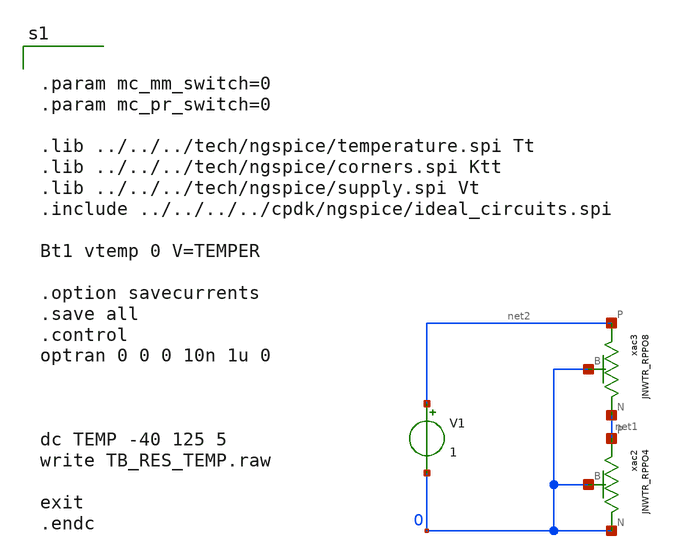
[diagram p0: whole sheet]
** sch_path: design/LELO_TEMP_SKY130A/TB_RES_TEMP.sch
**.subckt TB_RES_TEMP
xac2 0 net1 0 JNWTR_RPPO4 xoffset=0 yoffset=0 angle=0
xac3 net1 net2 0 JNWTR_RPPO8 xoffset=0 yoffset=0 angle=0 M=1
V1 net2 0 1
**** begin user architecture code


.param mc_mm_switch=0
.param mc_pr_switch=0

.lib ../../../tech/ngspice/temperature.spi Tt
.lib ../../../tech/ngspice/corners.spi Ktt
.lib ../../../tech/ngspice/supply.spi Vt
.include ../../../../cpdk/ngspice/ideal_circuits.spi

Bt1 vtemp 0 V=TEMPER

.option savecurrents
.save all
.control
optran 0 0 0 10n 1u 0



dc TEMP -40 125 5
write TB_RES_TEMP.raw

exit
.endc



**** end user architecture code
**.ends

* expanding   symbol:  JNW_TR_SKY130A/JNWTR_RPPO4.sym # of pins=3
** sym_path: JNW_TR_SKY130A/JNWTR_RPPO4.sym
** sch_path: JNW_TR_SKY130A/JNWTR_RPPO4.sch
.subckt JNWTR_RPPO4 N P B  xoffset=0 yoffset=0 angle=0
*.iopin P
*.iopin N
*.iopin B
XXA1 N P B JNWTR_RES4
.ends


* expanding   symbol:  JNW_TR_SKY130A/JNWTR_RPPO8.sym # of pins=3
** sym_path: JNW_TR_SKY130A/JNWTR_RPPO8.sym
** sch_path: JNW_TR_SKY130A/JNWTR_RPPO8.sch
.subckt JNWTR_RPPO8 N P B  xoffset=0 yoffset=0 angle=0 M=1
*.iopin P
*.iopin N
*.iopin B
XXA1 N P B JNWTR_RES8 xoffset=0 yoffset=0 angle=0
.ends


* expanding   symbol:  JNW_TR_SKY130A/JNWTR_RES4.sym # of pins=3
** sym_path: JNW_TR_SKY130A/JNWTR_RES4.sym
** sch_path: JNW_TR_SKY130A/JNWTR_RES4.sch
.subckt JNWTR_RES4 N P B
*.iopin N
*.iopin P
*.iopin B
XR1_0 INT_0 N B sky130_fd_pr__res_high_po W=0.36 L=7.2 mult=1 m=1
XR1_1 INT_1 INT_0 B sky130_fd_pr__res_high_po W=0.36 L=7.2 mult=1 m=1
XR1_2 INT_2 INT_1 B sky130_fd_pr__res_high_po W=0.36 L=7.2 mult=1 m=1
XR1_3 P INT_2 B sky130_fd_pr__res_high_po W=0.36 L=7.2 mult=1 m=1
.ends


* expanding   symbol:  JNW_TR_SKY130A/JNWTR_RES8.sym # of pins=3
** sym_path: JNW_TR_SKY130A/JNWTR_RES8.sym
** sch_path: JNW_TR_SKY130A/JNWTR_RES8.sch
.subckt JNWTR_RES8 N P B  xoffset=0 yoffset=0 angle=0
*.iopin N
*.iopin P
*.iopin B
XR1_0 INT_0 N B sky130_fd_pr__res_high_po W=0.36 L=7.2 mult=1 m=1
XR1_1 INT_1 INT_0 B sky130_fd_pr__res_high_po W=0.36 L=7.2 mult=1 m=1
XR1_2 INT_2 INT_1 B sky130_fd_pr__res_high_po W=0.36 L=7.2 mult=1 m=1
XR1_3 INT_3 INT_2 B sky130_fd_pr__res_high_po W=0.36 L=7.2 mult=1 m=1
XR1_4 INT_4 INT_3 B sky130_fd_pr__res_high_po W=0.36 L=7.2 mult=1 m=1
XR1_5 INT_5 INT_4 B sky130_fd_pr__res_high_po W=0.36 L=7.2 mult=1 m=1
XR1_6 INT_6 INT_5 B sky130_fd_pr__res_high_po W=0.36 L=7.2 mult=1 m=1
XR1_7 P INT_6 B sky130_fd_pr__res_high_po W=0.36 L=7.2 mult=1 m=1
.ends

.end
